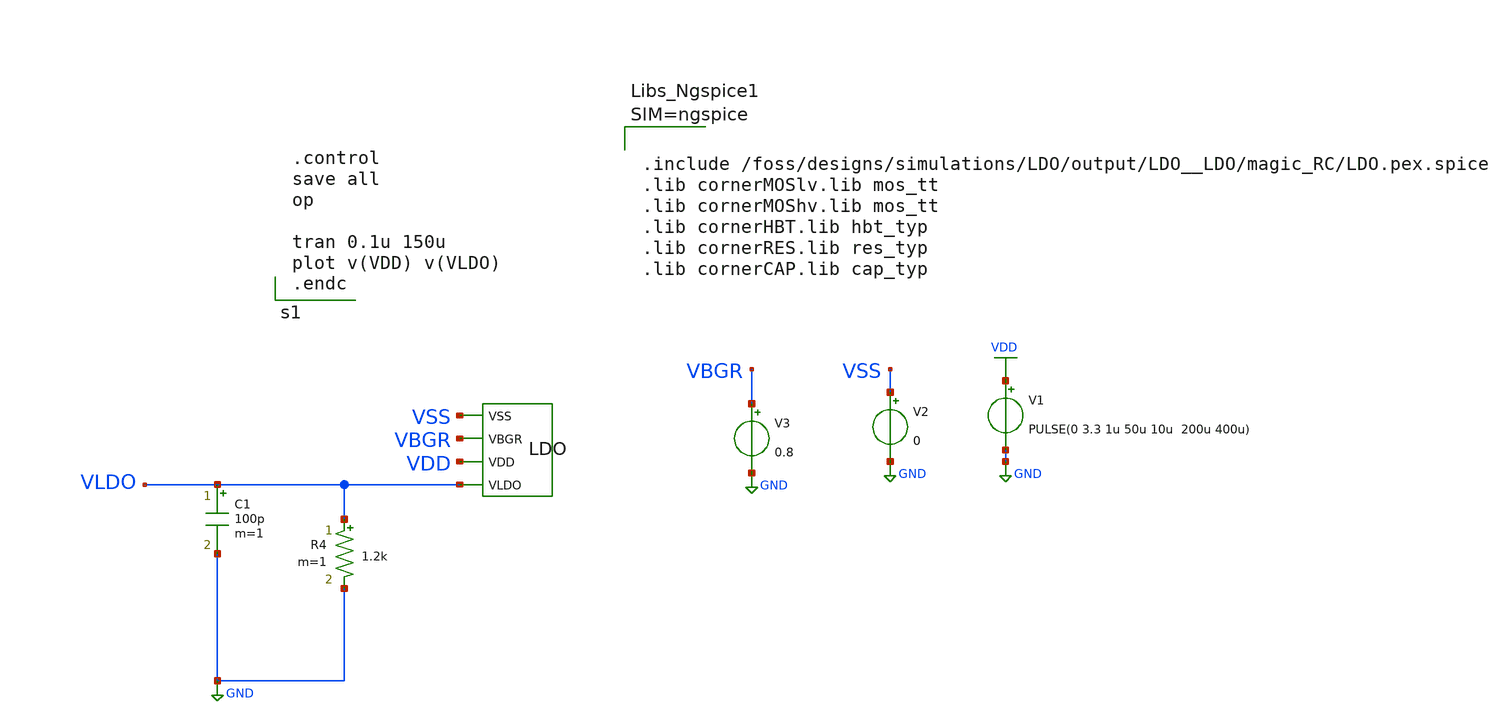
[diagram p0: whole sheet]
** sch_path: dependencies/LDO/LDO-main/testbenches/tran/xschem/ldo_post_layout_sim_Stratup_Value.sch
**.subckt ldo_post_layout_sim_Stratup_Value
V3 VBGR GND 0.8
V2 VSS GND 0
X1 VSS VBGR VDD VLDO LDO
C1 VLDO GND 100p m=1
R4 VLDO GND 1.2k m=1
V1 VDD GND PULSE(0 3.3 1u 50u 10u 200u 400u)
**** begin user architecture code



.include /foss/designs/simulations/LDO/output/LDO__LDO/magic_RC/LDO.pex.spice
.lib cornerMOSlv.lib mos_tt
.lib cornerMOShv.lib mos_tt
.lib cornerHBT.lib hbt_typ
.lib cornerRES.lib res_typ
.lib cornerCAP.lib cap_typ





.control
save all
op

tran 0.1u 150u
plot v(VDD) v(VLDO)
.endc

**** end user architecture code
**.ends
.GLOBAL GND
.GLOBAL VDD
.end
